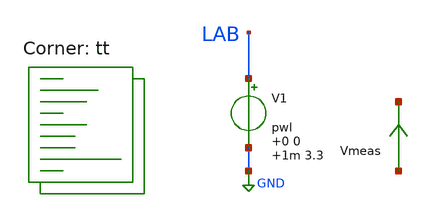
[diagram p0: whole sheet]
** sch_path: xschem/tb_template.sch
**.subckt tb_template
V1 LAB GND pwl 0 0 1m 3.3
Vmeas net1 net2 0
.save i(vmeas)
**** begin user architecture code
.lib $::SKYWATER_MODELS/sky130.lib.spice tt



.option chgtol=4e-16

*.param TEMPGAUSS = agauss(30, 40, 1)
*.option temp = 'TEMPGAUSS'
*.param DELTA = 0.002

.control
   setseed 3
   reset
   let run = 1
   save all
   op
   write RAW_FILE_NAME.raw
   reset
   set appendwrite
   dowhile run < 5
      save all
      tran 10u 1m uic
      write RAW_FILE_NAME.raw
      let run = run + 1
      reset
   end
.endc


**** end user architecture code
**.ends
.GLOBAL GND
.end
